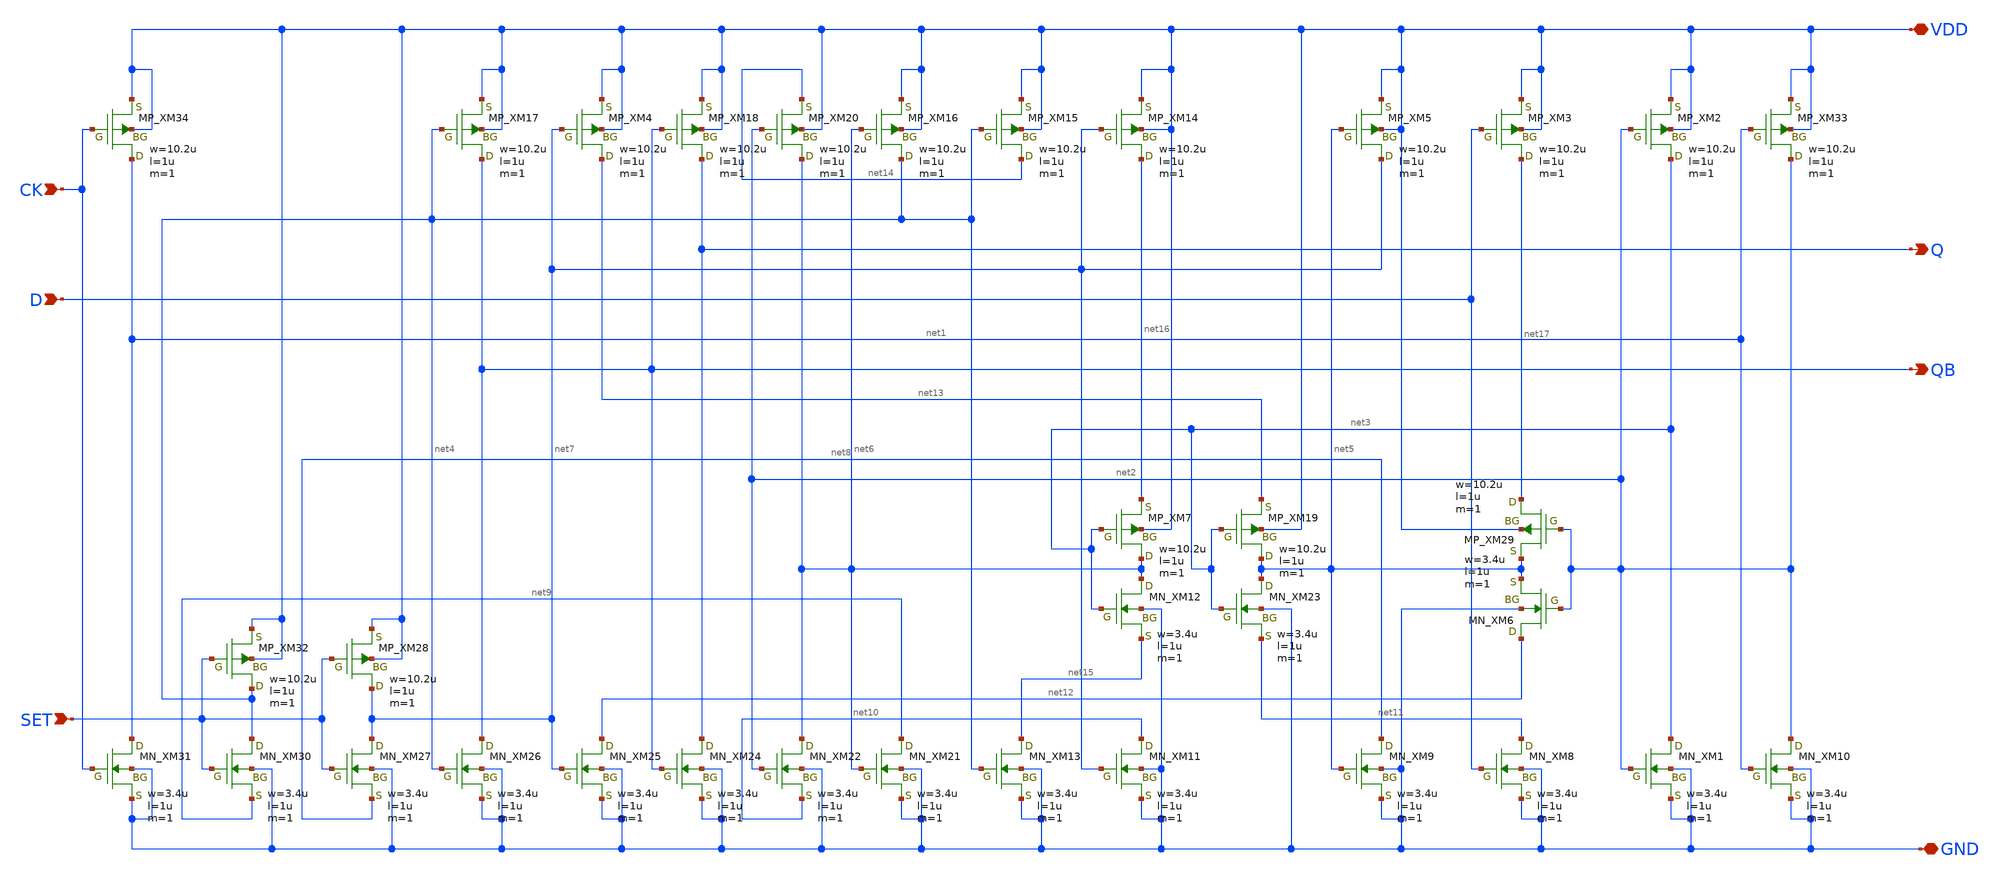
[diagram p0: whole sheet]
** sch_path: openIP62_rev1.0/IP62/Technology/tech/symbols/Xschem/IP62_5_stdcell/DFFS.sch
**.subckt DFFS CK Q SET D QB VDD GND
*.ipin CK
*.opin Q
*.ipin SET
*.ipin D
*.opin QB
*.iopin VDD
*.iopin GND
XM34 net1 CK VDD VDD PMOS w=10.2u l=1u as=0 ad=0 ps=0 pd=0 nrd=0 nrs=0 m=1
XM17 QB net4 VDD VDD PMOS w=10.2u l=1u as=0 ad=0 ps=0 pd=0 nrd=0 nrs=0 m=1
XM4 net13 net7 VDD VDD PMOS w=10.2u l=1u as=0 ad=0 ps=0 pd=0 nrd=0 nrs=0 m=1
XM18 Q QB VDD VDD PMOS w=10.2u l=1u as=0 ad=0 ps=0 pd=0 nrd=0 nrs=0 m=1
XM20 net6 net2 net14 VDD PMOS w=10.2u l=1u as=0 ad=0 ps=0 pd=0 nrd=0 nrs=0 m=1
XM16 net4 net6 VDD VDD PMOS w=10.2u l=1u as=0 ad=0 ps=0 pd=0 nrd=0 nrs=0 m=1
XM15 net14 net4 VDD VDD PMOS w=10.2u l=1u as=0 ad=0 ps=0 pd=0 nrd=0 nrs=0 m=1
XM14 net16 net7 VDD VDD PMOS w=10.2u l=1u as=0 ad=0 ps=0 pd=0 nrd=0 nrs=0 m=1
XM5 net7 net5 VDD VDD PMOS w=10.2u l=1u as=0 ad=0 ps=0 pd=0 nrd=0 nrs=0 m=1
XM3 net17 D VDD VDD PMOS w=10.2u l=1u as=0 ad=0 ps=0 pd=0 nrd=0 nrs=0 m=1
XM2 net3 net2 VDD VDD PMOS w=10.2u l=1u as=0 ad=0 ps=0 pd=0 nrd=0 nrs=0 m=1
XM33 net2 net1 VDD VDD PMOS w=10.2u l=1u as=0 ad=0 ps=0 pd=0 nrd=0 nrs=0 m=1
XM7 net6 net3 net16 VDD PMOS w=10.2u l=1u as=0 ad=0 ps=0 pd=0 nrd=0 nrs=0 m=1
XM19 net5 net3 net13 VDD PMOS w=10.2u l=1u as=0 ad=0 ps=0 pd=0 nrd=0 nrs=0 m=1
XM10 net2 net1 GND GND NMOS w=3.4u l=1u as=0 ad=0 ps=0 pd=0 nrd=0 nrs=0 m=1
XM1 net3 net2 GND GND NMOS w=3.4u l=1u as=0 ad=0 ps=0 pd=0 nrd=0 nrs=0 m=1
XM8 net11 D GND GND NMOS w=3.4u l=1u as=0 ad=0 ps=0 pd=0 nrd=0 nrs=0 m=1
XM9 net8 net5 GND GND NMOS w=3.4u l=1u as=0 ad=0 ps=0 pd=0 nrd=0 nrs=0 m=1
XM11 net10 net7 GND GND NMOS w=3.4u l=1u as=0 ad=0 ps=0 pd=0 nrd=0 nrs=0 m=1
XM13 net15 net4 GND GND NMOS w=3.4u l=1u as=0 ad=0 ps=0 pd=0 nrd=0 nrs=0 m=1
XM21 net9 net6 GND GND NMOS w=3.4u l=1u as=0 ad=0 ps=0 pd=0 nrd=0 nrs=0 m=1
XM22 net6 net2 net10 GND NMOS w=3.4u l=1u as=0 ad=0 ps=0 pd=0 nrd=0 nrs=0 m=1
XM24 Q QB GND GND NMOS w=3.4u l=1u as=0 ad=0 ps=0 pd=0 nrd=0 nrs=0 m=1
XM25 net12 net7 GND GND NMOS w=3.4u l=1u as=0 ad=0 ps=0 pd=0 nrd=0 nrs=0 m=1
XM26 QB net4 GND GND NMOS w=3.4u l=1u as=0 ad=0 ps=0 pd=0 nrd=0 nrs=0 m=1
XM27 net7 SET net8 GND NMOS w=3.4u l=1u as=0 ad=0 ps=0 pd=0 nrd=0 nrs=0 m=1
XM30 net4 SET net9 GND NMOS w=3.4u l=1u as=0 ad=0 ps=0 pd=0 nrd=0 nrs=0 m=1
XM31 net1 CK GND GND NMOS w=3.4u l=1u as=0 ad=0 ps=0 pd=0 nrd=0 nrs=0 m=1
XM32 net4 SET VDD VDD PMOS w=10.2u l=1u as=0 ad=0 ps=0 pd=0 nrd=0 nrs=0 m=1
XM28 net7 SET VDD VDD PMOS w=10.2u l=1u as=0 ad=0 ps=0 pd=0 nrd=0 nrs=0 m=1
XM12 net6 net3 net15 GND NMOS w=3.4u l=1u as=0 ad=0 ps=0 pd=0 nrd=0 nrs=0 m=1
XM23 net5 net3 net11 GND NMOS w=3.4u l=1u as=0 ad=0 ps=0 pd=0 nrd=0 nrs=0 m=1
XM29 net17 net2 net5 VDD PMOS w=10.2u l=1u as=0 ad=0 ps=0 pd=0 nrd=0 nrs=0 m=1
XM6 net12 net2 net5 GND NMOS w=3.4u l=1u as=0 ad=0 ps=0 pd=0 nrd=0 nrs=0 m=1
**.ends
.end
